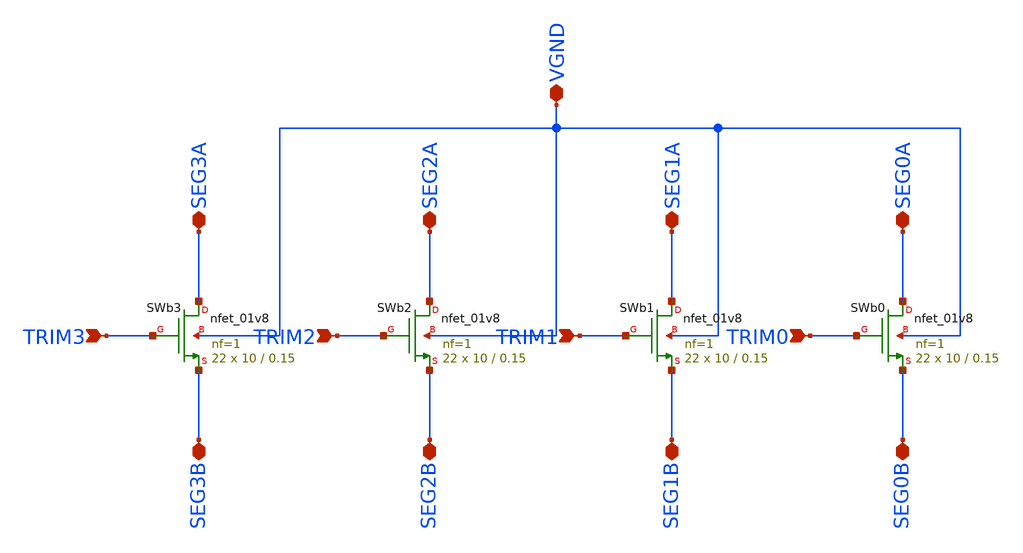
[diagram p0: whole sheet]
** sch_path: designs/bgr_ldo/bgr/trim_sw.sch
**.subckt trim_sw TRIM0 TRIM1 TRIM2 TRIM3 SEG0A SEG0B SEG1A SEG2A SEG3A SEG1B SEG2B SEG3B VGND
*.ipin TRIM0
*.ipin TRIM1
*.ipin TRIM2
*.ipin TRIM3
*.iopin SEG0A
*.iopin SEG0B
*.iopin SEG1A
*.iopin SEG2A
*.iopin SEG3A
*.iopin SEG1B
*.iopin SEG2B
*.iopin SEG3B
*.iopin VGND
XSWb0 SEG0A TRIM0 SEG0B VGND sky130_fd_pr__nfet_01v8 L=0.15 W=10 nf=1 ad='int((1 + 1)/2) * 10 / 1 * 0.29'
+ as='int((1 + 2)/2) * 10 / 1 * 0.29' pd='2*int((1 + 1)/2) * (10 / 1 + 0.29)' ps='2*int((1 + 2)/2) * (10 / 1 + 0.29)'
+ nrd='0.29 / 10 ' nrs='0.29 / 10 ' sa=0 sb=0 sd=0 mult=22 m=22
XSWb1 SEG1A TRIM1 SEG1B VGND sky130_fd_pr__nfet_01v8 L=0.15 W=10 nf=1 ad='int((1 + 1)/2) * 10 / 1 * 0.29'
+ as='int((1 + 2)/2) * 10 / 1 * 0.29' pd='2*int((1 + 1)/2) * (10 / 1 + 0.29)' ps='2*int((1 + 2)/2) * (10 / 1 + 0.29)'
+ nrd='0.29 / 10 ' nrs='0.29 / 10 ' sa=0 sb=0 sd=0 mult=22 m=22
XSWb2 SEG2A TRIM2 SEG2B VGND sky130_fd_pr__nfet_01v8 L=0.15 W=10 nf=1 ad='int((1 + 1)/2) * 10 / 1 * 0.29'
+ as='int((1 + 2)/2) * 10 / 1 * 0.29' pd='2*int((1 + 1)/2) * (10 / 1 + 0.29)' ps='2*int((1 + 2)/2) * (10 / 1 + 0.29)'
+ nrd='0.29 / 10 ' nrs='0.29 / 10 ' sa=0 sb=0 sd=0 mult=22 m=22
XSWb3 SEG3A TRIM3 SEG3B VGND sky130_fd_pr__nfet_01v8 L=0.15 W=10 nf=1 ad='int((1 + 1)/2) * 10 / 1 * 0.29'
+ as='int((1 + 2)/2) * 10 / 1 * 0.29' pd='2*int((1 + 1)/2) * (10 / 1 + 0.29)' ps='2*int((1 + 2)/2) * (10 / 1 + 0.29)'
+ nrd='0.29 / 10 ' nrs='0.29 / 10 ' sa=0 sb=0 sd=0 mult=22 m=22
**.ends
.end
